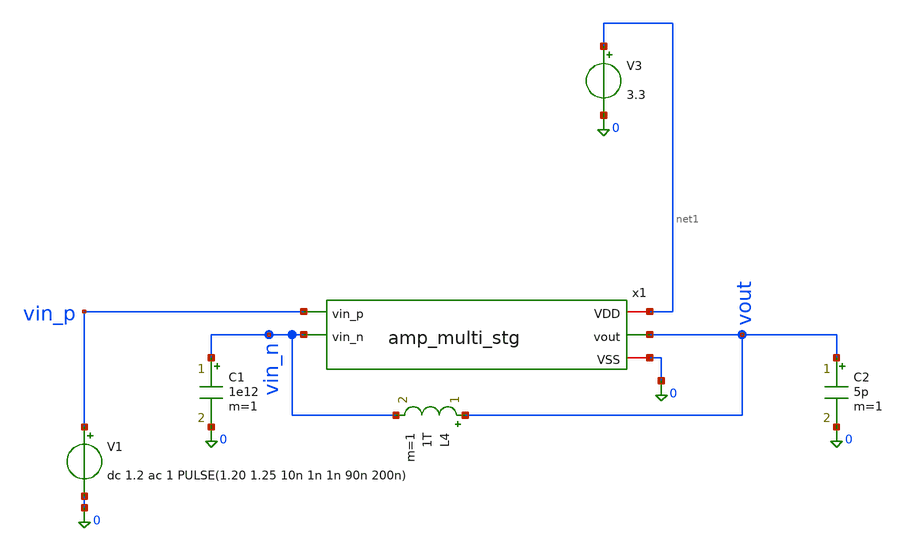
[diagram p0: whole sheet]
** sch_path: xschem/tb_amp_multi_stg_ac.sch
**.subckt tb_amp_multi_stg_ac
V3 net1 0 3.3
C2 vout 0 5p m=1
V1 vin_p 0 dc 1.2 ac 1 PULSE(1.20 1.25 10n 1n 1n 90n 200n)
L4 vout vin_n 1T m=1
C1 vin_n 0 1e12 m=1
x1 net1 vout 0 vin_p vin_n amp_multi_stg
**** begin user architecture code


* GF180MCU Global Process & Noise Parameters (Must be before .lib)
.param fnoicor = 0
.param sw_stat_global = 0
.param sw_stat_mismatch = 1

* PDK Model Include (MOSFETs)
.lib /foss/pdks/ciel/gf180mcu/versions/026824c7969ce6f4fc9678e6ca04b0a06a596c4b/gf180mcuD/libs.tech/ngspice/sm141064.ngspice typical

* MIM Capacitor Model (bypasses missing OSDI library)
.subckt cap_mim_2f0ff c0 c1 c_width=1e-6 c_length=1e-6
C_mim c0 c1 2.5p
.ends cap_mim_2f0ff

* Remove any .ac or .tran lines outside .control so they don't run prematurely
.save all

.control
* ======================================================================
* 1. DC OPERATING POINT & TRANSISTOR SATURATION CHECK
* ======================================================================
op

let v_inp_dc   = v(vin_p)
let v_inn_dc   = v(vin_n)
let v_out_dc   = v(vout)
let i_vdd_ua   = abs(v3#branch) * 1e6
let p_total_mw = i_vdd_ua * 3.3 / 1e3

echo ======================================================================
echo                   1. DC OPERATING VOLTAGES & POWER
echo ======================================================================
print v_inp_dc v_inn_dc v_out_dc
print i_vdd_ua p_total_mw

echo ======================================================================
echo                   2. TRANSISTOR SATURATION CHECK
echo ======================================================================
echo   If Margin is POSITIVE (+) -> SATURATION (GOOD)
echo   If Margin is NEGATIVE (-) -> TRIODE/LINEAR (BAD - KILLS GAIN)
echo ======================================================================

* NMOS Tail (XM3 in stg1)
let vds_tail   = abs(@m.x1.x2.xm3.m0[vds])
let vdsat_tail = abs(@m.x1.x2.xm3.m0[vdsat])
let marg_tail  = vds_tail - vdsat_tail

* NMOS Input (XM1 in stg1)
let vds_in     = abs(@m.x1.x2.xm1.m0[vds])
let vdsat_in   = abs(@m.x1.x2.xm1.m0[vdsat])
let marg_in    = vds_in - vdsat_in

* NMOS Cascode (XM4 in stg1)
let vds_casc   = abs(@m.x1.x2.xm4.m0[vds])
let vdsat_casc = abs(@m.x1.x2.xm4.m0[vdsat])
let marg_casc  = vds_casc - vdsat_casc

* PMOS Cascode (XM8 in stg1)
let vds_pcasc  = abs(@m.x1.x2.xm8.m0[vds])
let vdsat_pcasc= abs(@m.x1.x2.xm8.m0[vdsat])
let marg_pcasc = vds_pcasc - vdsat_pcasc

* PMOS Mirror (XM10 in stg1)
let vds_pmir   = abs(@m.x1.x2.xm10.m0[vds])
let vdsat_pmir = abs(@m.x1.x2.xm10.m0[vdsat])
let marg_pmir  = vds_pmir - vdsat_pmir

echo --- NMOS Tail (XM3) ---
print vds_tail vdsat_tail marg_tail
echo --- NMOS Input (XM1) ---
print vds_in vdsat_in marg_in
echo --- NMOS Cascode (XM4) ---
print vds_casc vdsat_casc marg_casc
echo --- PMOS Cascode (XM8) ---
print vds_pcasc vdsat_pcasc marg_pcasc
echo --- PMOS Mirror (XM10) ---
print vds_pmir vdsat_pmir marg_pmir
echo ======================================================================

* ======================================================================
* 3. AC FREQUENCY RESPONSE (OPEN-LOOP: L4=1e12, C1=1e12)
* ======================================================================
alter l4 = 1e12
alter c1 = 1e12
ac dec 35 1 5G

let v_out_ac  = v(vout)
let gain_db   = db(v_out_ac)
let phase_deg = cph(v_out_ac) * 180 / 3.1415926535

meas ac dc_gain find gain_db at=1
let g_3db = dc_gain - 3
meas ac f_3db when gain_db = g_3db
meas ac f_ugbw when gain_db = 0
meas ac ph_ugbw find phase_deg when gain_db = 0
let pm = 180 + ph_ugbw

echo ======================================================================
echo                   3. AC FREQUENCY RESPONSE RESULTS
echo ======================================================================
print dc_gain
print f_3db
print f_ugbw
print pm
echo ======================================================================

* ======================================================================
* 4. TRANSIENT & SLEW RATE (CLOSED-LOOP UNITY-GAIN: L4=1p, C1=1f)
* ======================================================================
alter l4 = 1e-12
alter c1 = 1e-18
tran 0.1n 1000n

meas tran v_init find v(vout) at=9n
meas tran v_max MAX v(vout) from=10n to=100n
meas tran v_min MIN v(vout) from=100n to=200n

* 20% to 80% levels (1.21V to 1.24V) with from=10n to ignore startup settling
meas tran t_rise TRIG v(vout) VAL=1.21 RISE=1 TARG v(vout) VAL=1.24 RISE=1 from=10n
meas tran t_fall TRIG v(vout) VAL=1.24 FALL=1 TARG v(vout) VAL=1.21 FALL=1 from=50n

* Calculate Slew Rates
let sr_rise_v_us = (0.03 / t_rise) / 1e6
let sr_fall_v_us = (0.03 / t_fall) / 1e6

echo ======================================================================
echo                   4. TRANSIENT & SLEW RATE RESULTS
echo ======================================================================
print v_init v_max v_min
print t_rise sr_rise_v_us
print t_fall sr_fall_v_us
echo ======================================================================

* ======================================================================
* 5. PLOTS
* ======================================================================
setplot ac1
plot db(v(vout)) title 'Open-Loop Gain (dB)'
plot (cph(v(vout))*180/3.14159265) title 'Open-Loop Phase (Deg)'

setplot tran1
plot v(vout) v(vin_p) title 'Closed-Loop Transient Step Response'
.endc


**** end user architecture code
**.ends

* expanding   symbol:  ttgf-ece298-analog-op-amp/xschem/amp_multi_stg.sym # of pins=5
** sym_path: xschem/amp_multi_stg.sym
** sch_path: xschem/amp_multi_stg.sch
.subckt amp_multi_stg VDD vout VSS vin_p vin_n
*.opin vout
*.ipin vin_n
*.ipin vin_p
*.iopin VSS
*.iopin VDD
x1 VDD net2 net3 net1 VSS amp_bias
x2 VDD net4 net2 net3 vin_p vin_n net1 VSS amp_stg_1
x3 VDD net4 vout net1 VSS amp_stg_2
.ends


* expanding   symbol:  ttgf-ece298-analog-op-amp/xschem/amp_bias.sym # of pins=5
** sym_path: xschem/amp_bias.sym
** sch_path: xschem/amp_bias.sch
.subckt amp_bias VDD vbias_1 vbias_2 vbias_mirror VSS
*.iopin VDD
*.iopin VSS
*.opin vbias_1
*.opin vbias_2
*.opin vbias_mirror
R1 VDD vbias_mirror 48.5k m=1
XM1 vbias_mirror vbias_mirror VSS VSS nfet_03v3 L=0.5u W=8u nf=1 ad='int((nf+1)/2) * W/nf * 0.18u' as='int((nf+2)/2)
+ * W/nf * 0.18u' pd='2*int((nf+1)/2) * (W/nf + 0.18u)' ps='2*int((nf+2)/2) * (W/nf + 0.18u)' nrd='0.18u
+ / W' nrs='0.18u / W' sa=0 sb=0 sd=0 m=1 par=1
XM3 net1 vbias_mirror VSS VSS nfet_03v3 L=1.4u W=8u nf=1 ad='int((nf+1)/2) * W/nf * 0.18u' as='int((nf+2)/2)
+ * W/nf * 0.18u' pd='2*int((nf+1)/2) * (W/nf + 0.18u)' ps='2*int((nf+2)/2) * (W/nf + 0.18u)' nrd='0.18u
+ / W' nrs='0.18u / W' sa=0 sb=0 sd=0 m=1 par=1
XM4 net1 net1 VDD VDD pfet_03v3 L=0.5u W=8u nf=1 ad='int((nf+1)/2) * W/nf * 0.18u' as='int((nf+2)/2)
+ * W/nf * 0.18u' pd='2*int((nf+1)/2) * (W/nf + 0.18u)' ps='2*int((nf+2)/2) * (W/nf + 0.18u)' nrd='0.18u
+ / W' nrs='0.18u / W' sa=0 sb=0 sd=0 m=1
XM5 vbias_2 net1 VDD VDD pfet_03v3 L=0.5u W=8u nf=1 ad='int((nf+1)/2) * W/nf * 0.18u' as='int((nf+2)/2)
+ * W/nf * 0.18u' pd='2*int((nf+1)/2) * (W/nf + 0.18u)' ps='2*int((nf+2)/2) * (W/nf + 0.18u)' nrd='0.18u
+ / W' nrs='0.18u / W' sa=0 sb=0 sd=0 m=1
XM6 vbias_1 vbias_mirror VSS VSS nfet_03v3 L=1.4u W=8u nf=1 ad='int((nf+1)/2) * W/nf * 0.18u' as='int((nf+2)/2)
+ * W/nf * 0.18u' pd='2*int((nf+1)/2) * (W/nf + 0.18u)' ps='2*int((nf+2)/2) * (W/nf + 0.18u)' nrd='0.18u
+ / W' nrs='0.18u / W' sa=0 sb=0 sd=0 m=1 par=1
XM7 net2 net2 VSS VSS nfet_03v3 L=0.5u W=14u nf=1 ad='int((nf+1)/2) * W/nf * 0.18u' as='int((nf+2)/2)
+ * W/nf * 0.18u' pd='2*int((nf+1)/2) * (W/nf + 0.18u)' ps='2*int((nf+2)/2) * (W/nf + 0.18u)' nrd='0.18u
+ / W' nrs='0.18u / W' sa=0 sb=0 sd=0 m=1 par=1
XM8 vbias_2 vbias_2 net2 VSS nfet_03v3 L=0.5u W=12u nf=1 ad='int((nf+1)/2) * W/nf * 0.18u' as='int((nf+2)/2)
+ * W/nf * 0.18u' pd='2*int((nf+1)/2) * (W/nf + 0.18u)' ps='2*int((nf+2)/2) * (W/nf + 0.18u)' nrd='0.18u
+ / W' nrs='0.18u / W' sa=0 sb=0 sd=0 m=1 par=1
XM9 vbias_1 vbias_1 VDD VDD pfet_03v3 L=1.4u W=2u nf=1 ad='int((nf+1)/2) * W/nf * 0.18u' as='int((nf+2)/2)
+ * W/nf * 0.18u' pd='2*int((nf+1)/2) * (W/nf + 0.18u)' ps='2*int((nf+2)/2) * (W/nf + 0.18u)' nrd='0.18u
+ / W' nrs='0.18u / W' sa=0 sb=0 sd=0 m=1
.ends


* expanding   symbol:  ttgf-ece298-analog-op-amp/xschem/amp_stg_1.sym # of pins=8
** sym_path: xschem/amp_stg_1.sym
** sch_path: xschem/amp_stg_1.sch
.subckt amp_stg_1 VDD vout vbias_1 vbias_2 vn vp vbias_tail VSS
*.iopin VDD
*.iopin VSS
*.ipin vn
*.ipin vp
*.opin vout
*.ipin vbias_tail
*.ipin vbias_2
*.ipin vbias_1
XM2 net3 vbias_1 net1 VDD pfet_03v3 L=2.0u W=28u nf=4 ad='int((nf+1)/2) * W/nf * 0.18u' as='int((nf+2)/2)
+ * W/nf * 0.18u' pd='2*int((nf+1)/2) * (W/nf + 0.18u)' ps='2*int((nf+2)/2) * (W/nf + 0.18u)' nrd='0.18u
+ / W' nrs='0.18u / W' sa=0 sb=0 sd=0 m=1 par=1
XM1 net4 vn net6 VSS nfet_03v3 L=1.4u W=16u nf=2 ad='int((nf+1)/2) * W/nf * 0.18u' as='int((nf+2)/2)
+ * W/nf * 0.18u' pd='2*int((nf+1)/2) * (W/nf + 0.18u)' ps='2*int((nf+2)/2) * (W/nf + 0.18u)' nrd='0.18u
+ / W' nrs='0.18u / W' sa=0 sb=0 sd=0 m=2 par=2
XM3 net6 vbias_tail VSS VSS nfet_03v3 L=1.4u W=32u nf=4 ad='int((nf+1)/2) * W/nf * 0.18u' as='int((nf+2)/2)
+ * W/nf * 0.18u' pd='2*int((nf+1)/2) * (W/nf + 0.18u)' ps='2*int((nf+2)/2) * (W/nf + 0.18u)' nrd='0.18u
+ / W' nrs='0.18u / W' sa=0 sb=0 sd=0 m=1 par=1
XM4 vout vbias_2 net4 VSS nfet_03v3 L=2.0u W=16u nf=4 ad='int((nf+1)/2) * W/nf * 0.18u' as='int((nf+2)/2)
+ * W/nf * 0.18u' pd='2*int((nf+1)/2) * (W/nf + 0.18u)' ps='2*int((nf+2)/2) * (W/nf + 0.18u)' nrd='0.18u
+ / W' nrs='0.18u / W' sa=0 sb=0 sd=0 m=1 par=1
XM5 net3 vbias_2 net5 VSS nfet_03v3 L=2.0u W=16u nf=4 ad='int((nf+1)/2) * W/nf * 0.18u' as='int((nf+2)/2)
+ * W/nf * 0.18u' pd='2*int((nf+1)/2) * (W/nf + 0.18u)' ps='2*int((nf+2)/2) * (W/nf + 0.18u)' nrd='0.18u
+ / W' nrs='0.18u / W' sa=0 sb=0 sd=0 m=1 par=1
XM7 net5 vp net6 VSS nfet_03v3 L=1.4u W=16u nf=2 ad='int((nf+1)/2) * W/nf * 0.18u' as='int((nf+2)/2)
+ * W/nf * 0.18u' pd='2*int((nf+1)/2) * (W/nf + 0.18u)' ps='2*int((nf+2)/2) * (W/nf + 0.18u)' nrd='0.18u
+ / W' nrs='0.18u / W' sa=0 sb=0 sd=0 m=2 par=2
XM8 vout vbias_1 net2 VDD pfet_03v3 L=2.0u W=28u nf=4 ad='int((nf+1)/2) * W/nf * 0.18u' as='int((nf+2)/2)
+ * W/nf * 0.18u' pd='2*int((nf+1)/2) * (W/nf + 0.18u)' ps='2*int((nf+2)/2) * (W/nf + 0.18u)' nrd='0.18u
+ / W' nrs='0.18u / W' sa=0 sb=0 sd=0 m=1 par=1
XM9 net1 net3 VDD VDD pfet_03v3 L=2.0u W=28u nf=4 ad='int((nf+1)/2) * W/nf * 0.18u' as='int((nf+2)/2)
+ * W/nf * 0.18u' pd='2*int((nf+1)/2) * (W/nf + 0.18u)' ps='2*int((nf+2)/2) * (W/nf + 0.18u)' nrd='0.18u
+ / W' nrs='0.18u / W' sa=0 sb=0 sd=0 m=1 par=1
XM10 net2 net3 VDD VDD pfet_03v3 L=2.0u W=28u nf=4 ad='int((nf+1)/2) * W/nf * 0.18u' as='int((nf+2)/2)
+ * W/nf * 0.18u' pd='2*int((nf+1)/2) * (W/nf + 0.18u)' ps='2*int((nf+2)/2) * (W/nf + 0.18u)' nrd='0.18u
+ / W' nrs='0.18u / W' sa=0 sb=0 sd=0 m=1 par=1
.ends


* expanding   symbol:  ttgf-ece298-analog-op-amp/xschem/amp_stg_2.sym # of pins=5
** sym_path: xschem/amp_stg_2.sym
** sch_path: xschem/amp_stg_2.sch
.subckt amp_stg_2 VDD vin vout vbias VSS
*.ipin vin
*.ipin vbias
*.iopin VSS
*.iopin VDD
*.opin vout
XM1 vout vin VDD VDD pfet_03v3 L=0.5u W=16u nf=1 ad='int((nf+1)/2) * W/nf * 0.18u' as='int((nf+2)/2)
+ * W/nf * 0.18u' pd='2*int((nf+1)/2) * (W/nf + 0.18u)' ps='2*int((nf+2)/2) * (W/nf + 0.18u)' nrd='0.18u
+ / W' nrs='0.18u / W' sa=0 sb=0 sd=0 m=1 par=1
XM5 vout vbias VSS VSS nfet_03v3 L=0.5u W=8.0u nf=1 ad='int((nf+1)/2) * W/nf * 0.18u' as='int((nf+2)/2)
+ * W/nf * 0.18u' pd='2*int((nf+1)/2) * (W/nf + 0.18u)' ps='2*int((nf+2)/2) * (W/nf + 0.18u)' nrd='0.18u
+ / W' nrs='0.18u / W' sa=0 sb=0 sd=0 m=1 par=1
C2 vin net1 3p m=1
R2 net1 vout 4.7k m=1
.ends

.end
